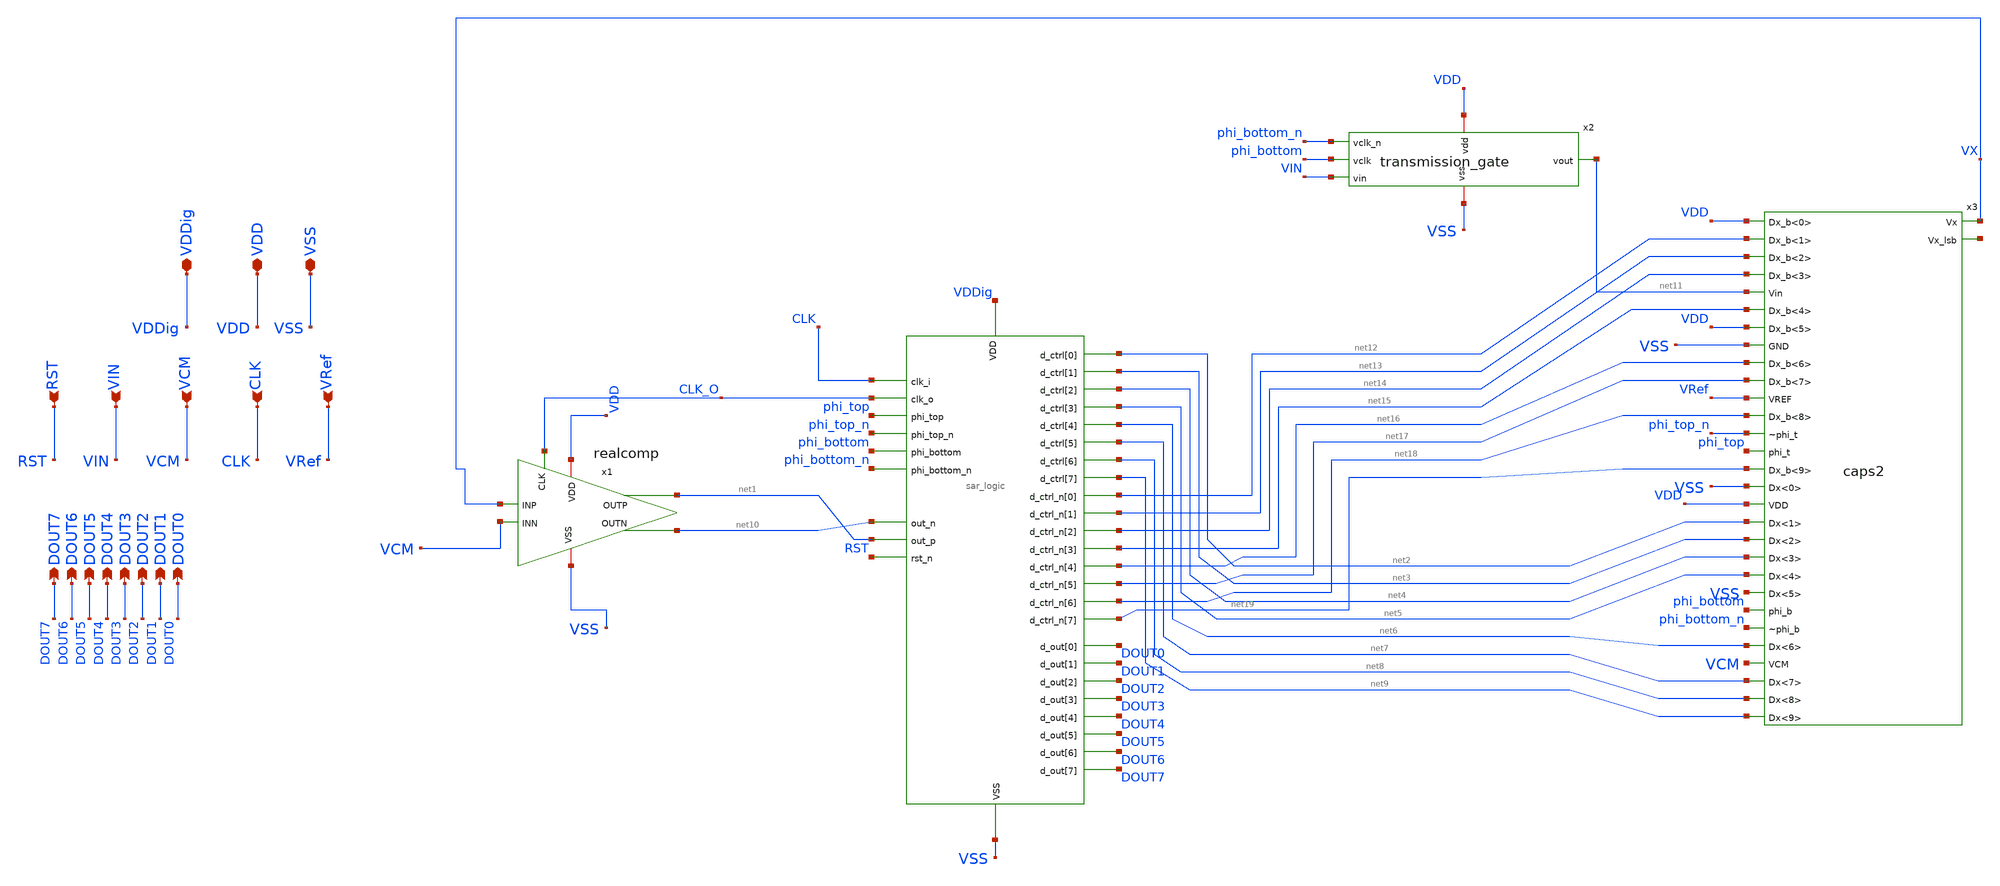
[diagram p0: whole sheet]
** sch_path: analog/top/top.sch
**.subckt top VSS VDD CLK VRef DOUT7 VCM VIN RST DOUT6 DOUT5 DOUT4 DOUT3 DOUT2 DOUT1 DOUT0 VDDig
*.iopin VSS
*.iopin VDD
*.ipin CLK
*.ipin VRef
*.opin DOUT7
*.ipin VCM
*.ipin VIN
*.ipin RST
*.opin DOUT6
*.opin DOUT5
*.opin DOUT4
*.opin DOUT3
*.opin DOUT2
*.opin DOUT1
*.opin DOUT0
*.iopin VDDig
x2 VDD net11 phi_bottom_n phi_bottom VIN VSS transmission_gate
X4 VDDig VSS CLK CLK_O net2 net3 net4 net5 net6 net7 net8 net9 net12 net13 net14 net15 net16 net17
+ net18 net19 DOUT0 DOUT1 DOUT2 DOUT3 DOUT4 DOUT5 DOUT6 DOUT7 net10 net1 phi_bottom phi_bottom_n phi_top
+ phi_top_n RST sar_adc_logic
x3 VDD net12 net13 net14 net11 net15 VDD VSS net16 net17 VRef net18 phi_top_n phi_top net19 VSS VDD
+ net2 VX net3 net4 net20 net5 VSS phi_bottom phi_bottom_n net6 VCM net7 net8 net9 caps2
x1 net10 net1 CLK_O VSS VDD VX VCM realcomp
**** begin user architecture code


.include /foss/designs/chipathon-2026-ti-adc/analog/digital/SAR_ADC_LOGIC/sar_adc_logic.spice
.include /foss/designs/chipathon-2026-ti-adc/analog/blocks/IDcomparator/IDcomparator.spice



.include $::180MCU_MODELS/design.ngspice
.include $PDK_ROOT/gf180mcuD/libs.ref/gf180mcu_fd_sc_mcu7t5v0/spice/gf180mcu_fd_sc_mcu7t5v0.spice
.lib $::180MCU_MODELS/sm141064.ngspice typical
.lib $::180MCU_MODELS/smbb000149.ngspice typical
.lib /foss/pdks/gf180mcuD/libs.tech/ngspice/sm141064.ngspice cap_mim
.lib /foss/pdks/gf180mcuD/libs.tech/ngspice/sm141064.ngspice mimcap_typical

**** end user architecture code
**.ends
.end
